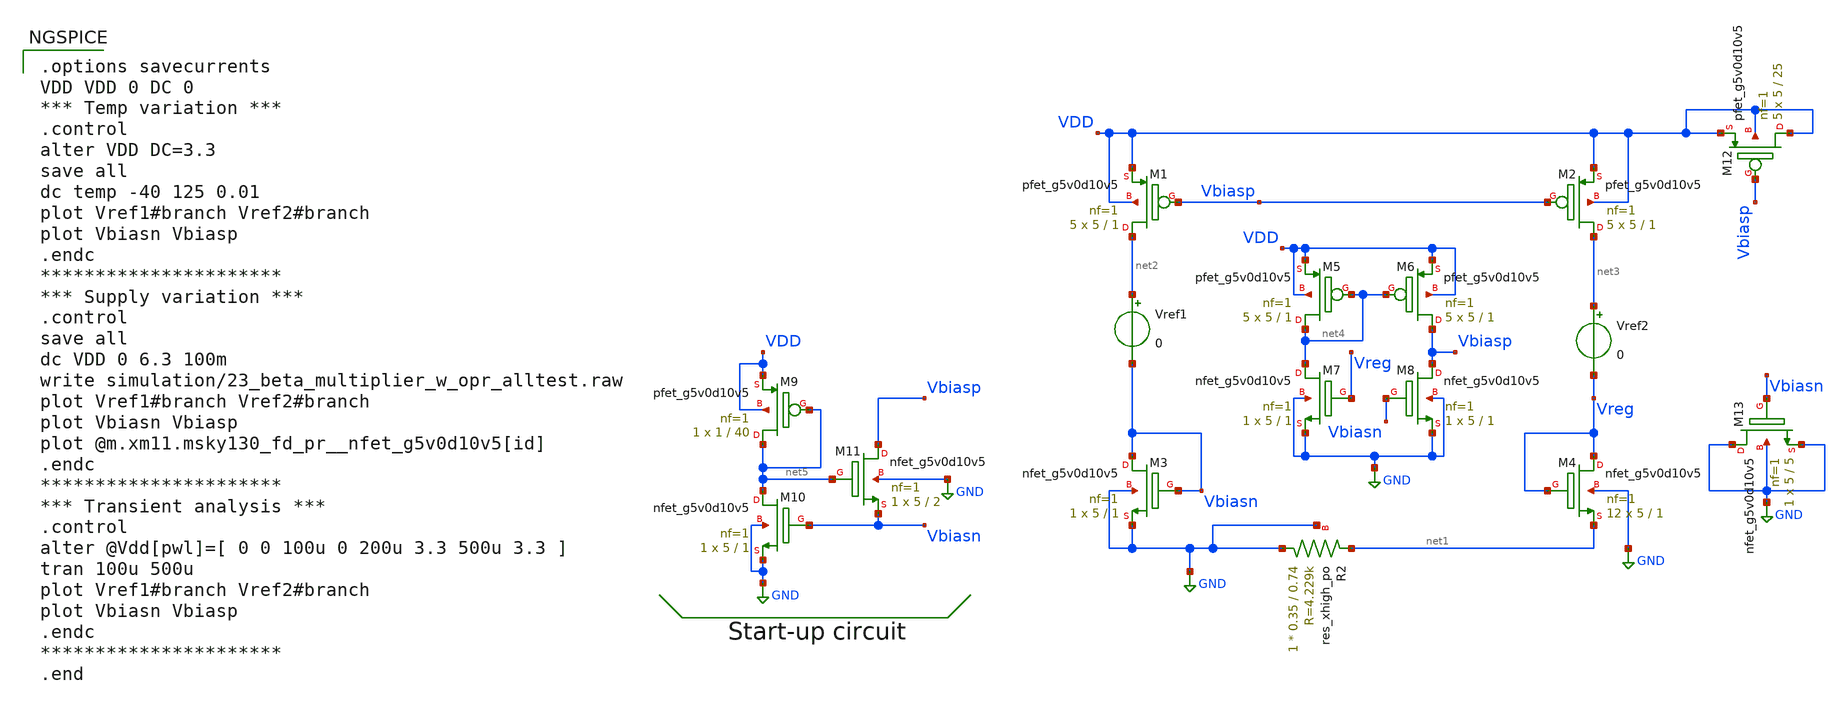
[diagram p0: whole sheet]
** sch_path: xschem/23_beta_multiplier_w_opr_alltest.sch
**.subckt 23_beta_multiplier_w_opr_alltest
XM1 net2 Vbiasp VDD VDD sky130_fd_pr__pfet_g5v0d10v5 L=1 W=5 nf=1 ad='int((nf+1)/2) * W/nf * 0.29' as='int((nf+2)/2) * W/nf * 0.29'
+ pd='2*int((nf+1)/2) * (W/nf + 0.29)' ps='2*int((nf+2)/2) * (W/nf + 0.29)' nrd='0.29 / W' nrs='0.29 / W'
+ sa=0 sb=0 sd=0 mult=5 m=5
XM3 Vbiasn Vbiasn GND GND sky130_fd_pr__nfet_g5v0d10v5 L=1 W=5 nf=1 ad='int((nf+1)/2) * W/nf * 0.29'
+ as='int((nf+2)/2) * W/nf * 0.29' pd='2*int((nf+1)/2) * (W/nf + 0.29)' ps='2*int((nf+2)/2) * (W/nf + 0.29)'
+ nrd='0.29 / W' nrs='0.29 / W' sa=0 sb=0 sd=0 mult=1 m=1
XM2 net3 Vbiasp VDD VDD sky130_fd_pr__pfet_g5v0d10v5 L=1 W=5 nf=1 ad='int((nf+1)/2) * W/nf * 0.29' as='int((nf+2)/2) * W/nf * 0.29'
+ pd='2*int((nf+1)/2) * (W/nf + 0.29)' ps='2*int((nf+2)/2) * (W/nf + 0.29)' nrd='0.29 / W' nrs='0.29 / W'
+ sa=0 sb=0 sd=0 mult=5 m=5
XM4 Vreg Vreg net1 GND sky130_fd_pr__nfet_g5v0d10v5 L=1 W=5 nf=1 ad='int((nf+1)/2) * W/nf * 0.29' as='int((nf+2)/2) * W/nf * 0.29'
+ pd='2*int((nf+1)/2) * (W/nf + 0.29)' ps='2*int((nf+2)/2) * (W/nf + 0.29)' nrd='0.29 / W' nrs='0.29 / W'
+ sa=0 sb=0 sd=0 mult=12 m=12
Vref1 net2 Vbiasn 0
Vref2 net3 Vreg 0
XR2 GND net1 GND sky130_fd_pr__res_xhigh_po W=0.35 L=0.74 mult=1 m=1
XM5 net4 net4 VDD VDD sky130_fd_pr__pfet_g5v0d10v5 L=1 W=5 nf=1 ad='int((nf+1)/2) * W/nf * 0.29' as='int((nf+2)/2) * W/nf * 0.29'
+ pd='2*int((nf+1)/2) * (W/nf + 0.29)' ps='2*int((nf+2)/2) * (W/nf + 0.29)' nrd='0.29 / W' nrs='0.29 / W'
+ sa=0 sb=0 sd=0 mult=5 m=5
XM6 Vbiasp net4 VDD VDD sky130_fd_pr__pfet_g5v0d10v5 L=1 W=5 nf=1 ad='int((nf+1)/2) * W/nf * 0.29' as='int((nf+2)/2) * W/nf * 0.29'
+ pd='2*int((nf+1)/2) * (W/nf + 0.29)' ps='2*int((nf+2)/2) * (W/nf + 0.29)' nrd='0.29 / W' nrs='0.29 / W'
+ sa=0 sb=0 sd=0 mult=5 m=5
XM7 net4 Vreg GND GND sky130_fd_pr__nfet_g5v0d10v5 L=1 W=5 nf=1 ad='int((nf+1)/2) * W/nf * 0.29' as='int((nf+2)/2) * W/nf * 0.29'
+ pd='2*int((nf+1)/2) * (W/nf + 0.29)' ps='2*int((nf+2)/2) * (W/nf + 0.29)' nrd='0.29 / W' nrs='0.29 / W'
+ sa=0 sb=0 sd=0 mult=1 m=1
XM8 Vbiasp Vbiasn GND GND sky130_fd_pr__nfet_g5v0d10v5 L=1 W=5 nf=1 ad='int((nf+1)/2) * W/nf * 0.29'
+ as='int((nf+2)/2) * W/nf * 0.29' pd='2*int((nf+1)/2) * (W/nf + 0.29)' ps='2*int((nf+2)/2) * (W/nf + 0.29)'
+ nrd='0.29 / W' nrs='0.29 / W' sa=0 sb=0 sd=0 mult=1 m=1
XM9 net5 net5 VDD VDD sky130_fd_pr__pfet_g5v0d10v5 L=40 W=1 nf=1 ad='int((nf+1)/2) * W/nf * 0.29' as='int((nf+2)/2) * W/nf * 0.29'
+ pd='2*int((nf+1)/2) * (W/nf + 0.29)' ps='2*int((nf+2)/2) * (W/nf + 0.29)' nrd='0.29 / W' nrs='0.29 / W'
+ sa=0 sb=0 sd=0 mult=1 m=1
XM10 net5 Vbiasn GND GND sky130_fd_pr__nfet_g5v0d10v5 L=1 W=5 nf=1 ad='int((nf+1)/2) * W/nf * 0.29' as='int((nf+2)/2) * W/nf * 0.29'
+ pd='2*int((nf+1)/2) * (W/nf + 0.29)' ps='2*int((nf+2)/2) * (W/nf + 0.29)' nrd='0.29 / W' nrs='0.29 / W'
+ sa=0 sb=0 sd=0 mult=1 m=1
XM11 Vbiasp net5 Vbiasn GND sky130_fd_pr__nfet_g5v0d10v5 L=2 W=5 nf=1 ad='int((nf+1)/2) * W/nf * 0.29'
+ as='int((nf+2)/2) * W/nf * 0.29' pd='2*int((nf+1)/2) * (W/nf + 0.29)' ps='2*int((nf+2)/2) * (W/nf + 0.29)'
+ nrd='0.29 / W' nrs='0.29 / W' sa=0 sb=0 sd=0 mult=1 m=1
XM12 VDD Vbiasp VDD VDD sky130_fd_pr__pfet_g5v0d10v5 L=25 W=5 nf=1 ad='int((nf+1)/2) * W/nf * 0.29' as='int((nf+2)/2) * W/nf * 0.29'
+ pd='2*int((nf+1)/2) * (W/nf + 0.29)' ps='2*int((nf+2)/2) * (W/nf + 0.29)' nrd='0.29 / W' nrs='0.29 / W'
+ sa=0 sb=0 sd=0 mult=5 m=5
XM13 GND Vbiasn GND GND sky130_fd_pr__nfet_g5v0d10v5 L=5 W=5 nf=1 ad='int((nf+1)/2) * W/nf * 0.29' as='int((nf+2)/2) * W/nf * 0.29'
+ pd='2*int((nf+1)/2) * (W/nf + 0.29)' ps='2*int((nf+2)/2) * (W/nf + 0.29)' nrd='0.29 / W' nrs='0.29 / W'
+ sa=0 sb=0 sd=0 mult=1 m=1
**** begin user architecture code

.options savecurrents
VDD VDD 0 DC 0
*** Temp variation ***
.control
alter VDD DC=3.3
save all
dc temp -40 125 0.01
plot Vref1#branch Vref2#branch
plot Vbiasn Vbiasp
.endc
**********************
*** Supply variation ***
.control
save all
dc VDD 0 6.3 100m
write simulation/23_beta_multiplier_w_opr_alltest.raw
plot Vref1#branch Vref2#branch
plot Vbiasn Vbiasp
plot @m.xm11.msky130_fd_pr__nfet_g5v0d10v5[id]
.endc
**********************
*** Transient analysis ***
.control
alter @Vdd[pwl]=[ 0 0 100u 0 200u 3.3 500u 3.3 ]
tran 100u 500u
plot Vref1#branch Vref2#branch
plot Vbiasn Vbiasp
.endc
**********************
.end


** opencircuitdesign pdks install
.lib $::SKYWATER_MODELS/sky130.lib.spice tt


**** end user architecture code
**.ends
.GLOBAL GND
.end
